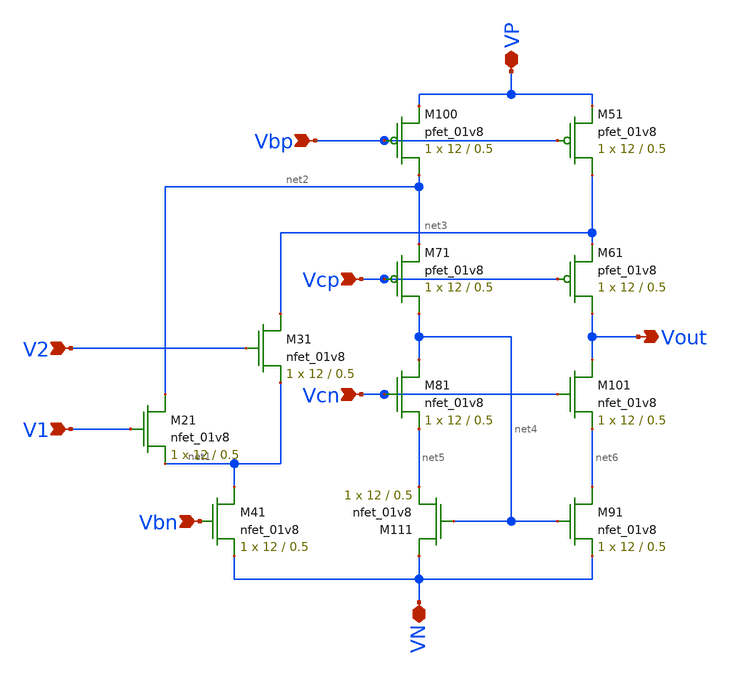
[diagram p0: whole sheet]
** sch_path: mp3/schematic/fcda.sch
**.subckt fcda VP VN Vbp V2 V1 Vbn Vcp Vcn Vout
*.iopin VP
*.iopin VN
*.ipin Vbp
*.ipin V2
*.ipin V1
*.ipin Vbn
*.ipin Vcp
*.ipin Vcn
*.opin Vout
XM100 net2 Vbp VP VDD sky130_fd_pr__pfet_01v8 L=0.5 W=12 nf=1 ad='int((nf+1)/2) * W/nf * 0.29' as='int((nf+2)/2) * W/nf * 0.29'
+ pd='2*int((nf+1)/2) * (W/nf + 0.29)' ps='2*int((nf+2)/2) * (W/nf + 0.29)' nrd='0.29 / W' nrs='0.29 / W'
+ sa=0 sb=0 sd=0 mult=1 m=1
XM21 net2 V1 net1 GND sky130_fd_pr__nfet_01v8 L=0.5 W=12 nf=1 ad='int((nf+1)/2) * W/nf * 0.29' as='int((nf+2)/2) * W/nf * 0.29'
+ pd='2*int((nf+1)/2) * (W/nf + 0.29)' ps='2*int((nf+2)/2) * (W/nf + 0.29)' nrd='0.29 / W' nrs='0.29 / W'
+ sa=0 sb=0 sd=0 mult=1 m=1
XM31 net3 V2 net1 GND sky130_fd_pr__nfet_01v8 L=0.5 W=12 nf=1 ad='int((nf+1)/2) * W/nf * 0.29' as='int((nf+2)/2) * W/nf * 0.29'
+ pd='2*int((nf+1)/2) * (W/nf + 0.29)' ps='2*int((nf+2)/2) * (W/nf + 0.29)' nrd='0.29 / W' nrs='0.29 / W'
+ sa=0 sb=0 sd=0 mult=1 m=1
XM41 net1 Vbn VN GND sky130_fd_pr__nfet_01v8 L=0.5 W=12 nf=1 ad='int((nf+1)/2) * W/nf * 0.29' as='int((nf+2)/2) * W/nf * 0.29'
+ pd='2*int((nf+1)/2) * (W/nf + 0.29)' ps='2*int((nf+2)/2) * (W/nf + 0.29)' nrd='0.29 / W' nrs='0.29 / W'
+ sa=0 sb=0 sd=0 mult=1 m=1
XM51 net3 Vbp VP VDD sky130_fd_pr__pfet_01v8 L=0.5 W=12 nf=1 ad='int((nf+1)/2) * W/nf * 0.29' as='int((nf+2)/2) * W/nf * 0.29'
+ pd='2*int((nf+1)/2) * (W/nf + 0.29)' ps='2*int((nf+2)/2) * (W/nf + 0.29)' nrd='0.29 / W' nrs='0.29 / W'
+ sa=0 sb=0 sd=0 mult=1 m=1
XM61 Vout Vcp net3 VDD sky130_fd_pr__pfet_01v8 L=0.5 W=12 nf=1 ad='int((nf+1)/2) * W/nf * 0.29' as='int((nf+2)/2) * W/nf * 0.29'
+ pd='2*int((nf+1)/2) * (W/nf + 0.29)' ps='2*int((nf+2)/2) * (W/nf + 0.29)' nrd='0.29 / W' nrs='0.29 / W'
+ sa=0 sb=0 sd=0 mult=1 m=1
XM71 net4 Vcp net2 VDD sky130_fd_pr__pfet_01v8 L=0.5 W=12 nf=1 ad='int((nf+1)/2) * W/nf * 0.29' as='int((nf+2)/2) * W/nf * 0.29'
+ pd='2*int((nf+1)/2) * (W/nf + 0.29)' ps='2*int((nf+2)/2) * (W/nf + 0.29)' nrd='0.29 / W' nrs='0.29 / W'
+ sa=0 sb=0 sd=0 mult=1 m=1
XM81 net4 Vcn net5 GND sky130_fd_pr__nfet_01v8 L=0.5 W=12 nf=1 ad='int((nf+1)/2) * W/nf * 0.29' as='int((nf+2)/2) * W/nf * 0.29'
+ pd='2*int((nf+1)/2) * (W/nf + 0.29)' ps='2*int((nf+2)/2) * (W/nf + 0.29)' nrd='0.29 / W' nrs='0.29 / W'
+ sa=0 sb=0 sd=0 mult=1 m=1
XM91 net6 net4 VN GND sky130_fd_pr__nfet_01v8 L=0.5 W=12 nf=1 ad='int((nf+1)/2) * W/nf * 0.29' as='int((nf+2)/2) * W/nf * 0.29'
+ pd='2*int((nf+1)/2) * (W/nf + 0.29)' ps='2*int((nf+2)/2) * (W/nf + 0.29)' nrd='0.29 / W' nrs='0.29 / W'
+ sa=0 sb=0 sd=0 mult=1 m=1
XM101 Vout Vcn net6 GND sky130_fd_pr__nfet_01v8 L=0.5 W=12 nf=1 ad='int((nf+1)/2) * W/nf * 0.29' as='int((nf+2)/2) * W/nf * 0.29'
+ pd='2*int((nf+1)/2) * (W/nf + 0.29)' ps='2*int((nf+2)/2) * (W/nf + 0.29)' nrd='0.29 / W' nrs='0.29 / W'
+ sa=0 sb=0 sd=0 mult=1 m=1
XM111 VN net4 net5 GND sky130_fd_pr__nfet_01v8 L=0.5 W=12 nf=1 ad='int((nf+1)/2) * W/nf * 0.29' as='int((nf+2)/2) * W/nf * 0.29'
+ pd='2*int((nf+1)/2) * (W/nf + 0.29)' ps='2*int((nf+2)/2) * (W/nf + 0.29)' nrd='0.29 / W' nrs='0.29 / W'
+ sa=0 sb=0 sd=0 mult=1 m=1
**.ends
.end
